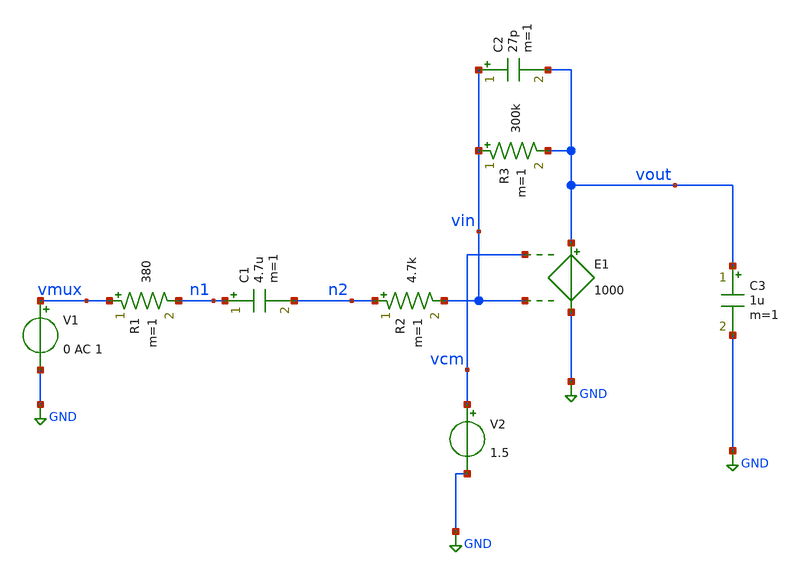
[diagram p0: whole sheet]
** sch_path: untitled.sch
**.subckt untitled
V1 vmux GND 0 AC 1
R1 vmux n1 380 m=1
C1 n1 n2 4.7u m=1
R2 n2 vin 4.7k m=1
E1 vout GND vcm vin 1000
C2 vin vout 27p m=1
R3 vin vout 300k m=1
V2 vcm GND 1.5
C3 vout GND 1u m=1
**.ends
.GLOBAL GND
.end
